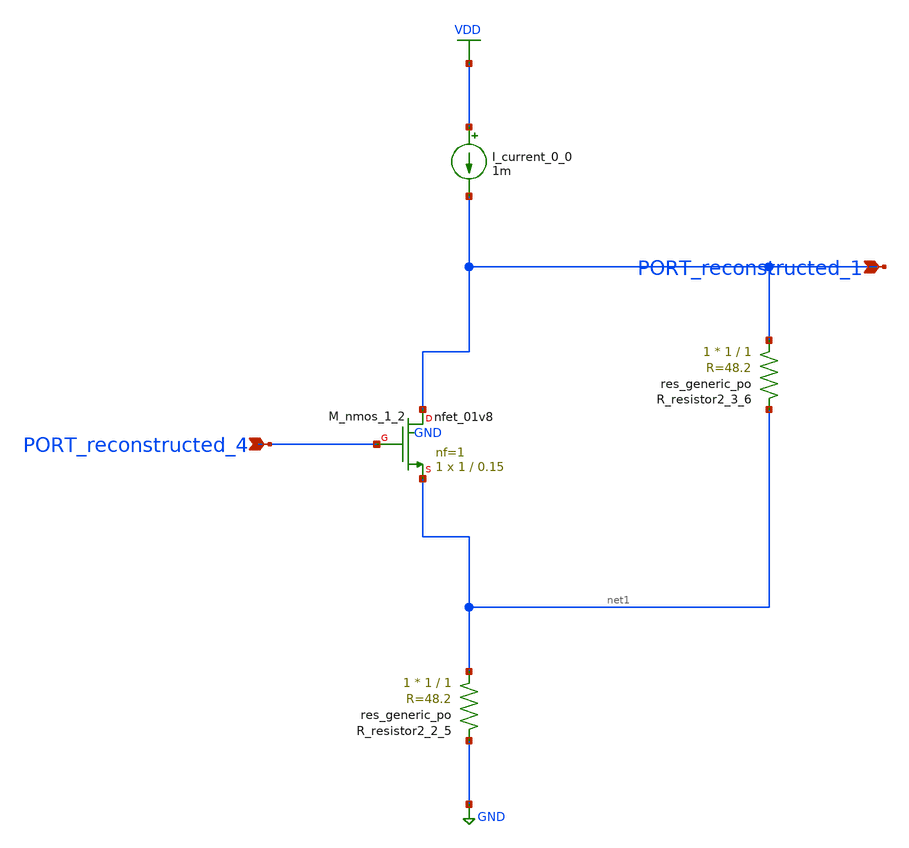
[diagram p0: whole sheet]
** sch_path: schematics/AMSNet/508.sch
**.subckt 508 PORT_reconstructed_4 PORT_reconstructed_1
*.ipin PORT_reconstructed_4
*.ipin PORT_reconstructed_1
I_current_0_0 VDD PORT_reconstructed_1 1m
XM_nmos_1_2 PORT_reconstructed_1 PORT_reconstructed_4 net1 GND sky130_fd_pr__nfet_01v8 L=0.15 W=1 nf=1
+ ad='int((1 + 1)/2) * 1 / 1 * 0.29' as='int((1 + 2)/2) * 1 / 1 * 0.29' pd='2*int((1 + 1)/2) * (1 / 1 + 0.29)'
+ ps='2*int((1 + 2)/2) * (1 / 1 + 0.29)' nrd='0.29 / 1 ' nrs='0.29 / 1 ' sa=0 sb=0 sd=0 mult=1 m=1
XR_resistor2_2_5 net1 GND sky130_fd_pr__res_generic_po W=1 L=1 m=1
XR_resistor2_3_6 PORT_reconstructed_1 net1 sky130_fd_pr__res_generic_po W=1 L=1 m=1
**.ends
.GLOBAL GND
.GLOBAL VDD
.end
